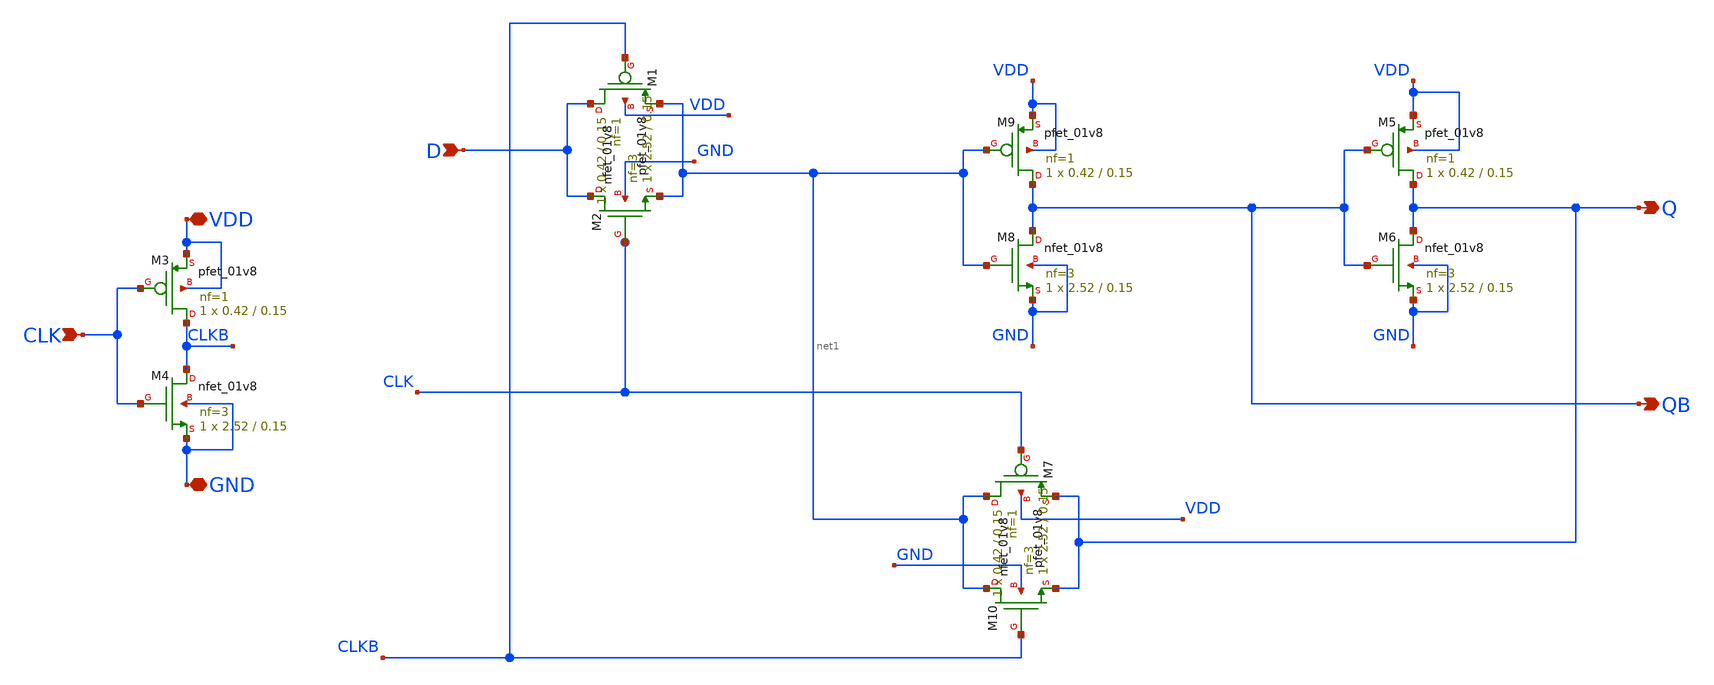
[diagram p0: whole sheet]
** sch_path: cells/DLX1/schematic/dlx1.sch
**.subckt dlx1 D VDD GND CLK QB Q
*.ipin D
*.iopin VDD
*.iopin GND
*.ipin CLK
*.opin QB
*.opin Q
XM1 D CLKB net1 VDD sky130_fd_pr__pfet_01v8 L=0.15 W=0.42 nf=1 ad='int((1 + 1)/2) * 0.42 / 1 * 0.29'
+ as='int((1 + 2)/2) * 0.42 / 1 * 0.29' pd='2*int((1 + 1)/2) * (0.42 / 1 + 0.29)' ps='2*int((1 + 2)/2) * (0.42 / 1 + 0.29)'
+ nrd='0.29 / 0.42 ' nrs='0.29 / 0.42 ' sa=0 sb=0 sd=0 mult=1 m=1
XM2 D CLK net1 GND sky130_fd_pr__nfet_01v8 L=0.15 W=2.52 nf=3 ad='int((3 + 1)/2) * 2.52 / 3 * 0.29' as='int((3 + 2)/2) * 2.52 / 3 * 0.29'
+ pd='2*int((3 + 1)/2) * (2.52 / 3 + 0.29)' ps='2*int((3 + 2)/2) * (2.52 / 3 + 0.29)' nrd='0.29 / 2.52 '
+ nrs='0.29 / 2.52 ' sa=0 sb=0 sd=0 mult=1 m=1
XM3 CLKB CLK VDD VDD sky130_fd_pr__pfet_01v8 L=0.15 W=0.42 nf=1 ad='int((1 + 1)/2) * 0.42 / 1 * 0.29'
+ as='int((1 + 2)/2) * 0.42 / 1 * 0.29' pd='2*int((1 + 1)/2) * (0.42 / 1 + 0.29)' ps='2*int((1 + 2)/2) * (0.42 / 1 + 0.29)'
+ nrd='0.29 / 0.42 ' nrs='0.29 / 0.42 ' sa=0 sb=0 sd=0 mult=1 m=1
XM4 CLKB CLK GND GND sky130_fd_pr__nfet_01v8 L=0.15 W=2.52 nf=3 ad='int((3 + 1)/2) * 2.52 / 3 * 0.29'
+ as='int((3 + 2)/2) * 2.52 / 3 * 0.29' pd='2*int((3 + 1)/2) * (2.52 / 3 + 0.29)' ps='2*int((3 + 2)/2) * (2.52 / 3 + 0.29)'
+ nrd='0.29 / 2.52 ' nrs='0.29 / 2.52 ' sa=0 sb=0 sd=0 mult=1 m=1
XM9 QB net1 VDD VDD sky130_fd_pr__pfet_01v8 L=0.15 W=0.42 nf=1 ad='int((1 + 1)/2) * 0.42 / 1 * 0.29'
+ as='int((1 + 2)/2) * 0.42 / 1 * 0.29' pd='2*int((1 + 1)/2) * (0.42 / 1 + 0.29)' ps='2*int((1 + 2)/2) * (0.42 / 1 + 0.29)'
+ nrd='0.29 / 0.42 ' nrs='0.29 / 0.42 ' sa=0 sb=0 sd=0 mult=1 m=1
XM8 QB net1 GND GND sky130_fd_pr__nfet_01v8 L=0.15 W=2.52 nf=3 ad='int((3 + 1)/2) * 2.52 / 3 * 0.29'
+ as='int((3 + 2)/2) * 2.52 / 3 * 0.29' pd='2*int((3 + 1)/2) * (2.52 / 3 + 0.29)' ps='2*int((3 + 2)/2) * (2.52 / 3 + 0.29)'
+ nrd='0.29 / 2.52 ' nrs='0.29 / 2.52 ' sa=0 sb=0 sd=0 mult=1 m=1
XM5 Q QB VDD VDD sky130_fd_pr__pfet_01v8 L=0.15 W=0.42 nf=1 ad='int((1 + 1)/2) * 0.42 / 1 * 0.29' as='int((1 + 2)/2) * 0.42 / 1 * 0.29'
+ pd='2*int((1 + 1)/2) * (0.42 / 1 + 0.29)' ps='2*int((1 + 2)/2) * (0.42 / 1 + 0.29)' nrd='0.29 / 0.42 '
+ nrs='0.29 / 0.42 ' sa=0 sb=0 sd=0 mult=1 m=1
XM6 Q QB GND GND sky130_fd_pr__nfet_01v8 L=0.15 W=2.52 nf=3 ad='int((3 + 1)/2) * 2.52 / 3 * 0.29' as='int((3 + 2)/2) * 2.52 / 3 * 0.29'
+ pd='2*int((3 + 1)/2) * (2.52 / 3 + 0.29)' ps='2*int((3 + 2)/2) * (2.52 / 3 + 0.29)' nrd='0.29 / 2.52 '
+ nrs='0.29 / 2.52 ' sa=0 sb=0 sd=0 mult=1 m=1
XM7 net1 CLK Q VDD sky130_fd_pr__pfet_01v8 L=0.15 W=0.42 nf=1 ad='int((1 + 1)/2) * 0.42 / 1 * 0.29' as='int((1 + 2)/2) * 0.42 / 1 * 0.29'
+ pd='2*int((1 + 1)/2) * (0.42 / 1 + 0.29)' ps='2*int((1 + 2)/2) * (0.42 / 1 + 0.29)' nrd='0.29 / 0.42 '
+ nrs='0.29 / 0.42 ' sa=0 sb=0 sd=0 mult=1 m=1
XM10 net1 CLKB Q GND sky130_fd_pr__nfet_01v8 L=0.15 W=2.52 nf=3 ad='int((3 + 1)/2) * 2.52 / 3 * 0.29'
+ as='int((3 + 2)/2) * 2.52 / 3 * 0.29' pd='2*int((3 + 1)/2) * (2.52 / 3 + 0.29)' ps='2*int((3 + 2)/2) * (2.52 / 3 + 0.29)'
+ nrd='0.29 / 2.52 ' nrs='0.29 / 2.52 ' sa=0 sb=0 sd=0 mult=1 m=1
**.ends
.end
